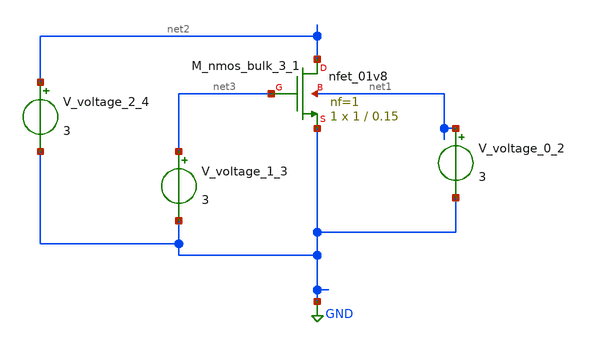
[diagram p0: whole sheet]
** sch_path: schematics/10_5573_IEIESPC_2014_3_6_425_02_004.sch
**.subckt 10_5573_IEIESPC_2014_3_6_425_02_004
XM_nmos_bulk_3_1 net2 net3 GND net1 sky130_fd_pr__nfet_01v8 L=0.15 W=1 nf=1 ad='int((1 + 1)/2) * 1 / 1 * 0.29'
+ as='int((1 + 2)/2) * 1 / 1 * 0.29' pd='2*int((1 + 1)/2) * (1 / 1 + 0.29)' ps='2*int((1 + 2)/2) * (1 / 1 + 0.29)'
+ nrd='0.29 / 1 ' nrs='0.29 / 1 ' sa=0 sb=0 sd=0 mult=1 m=1
V_voltage_0_2 net1 GND 3
V_voltage_1_3 net3 GND 3
V_voltage_2_4 net2 GND 3
**.ends
.GLOBAL GND
.end
